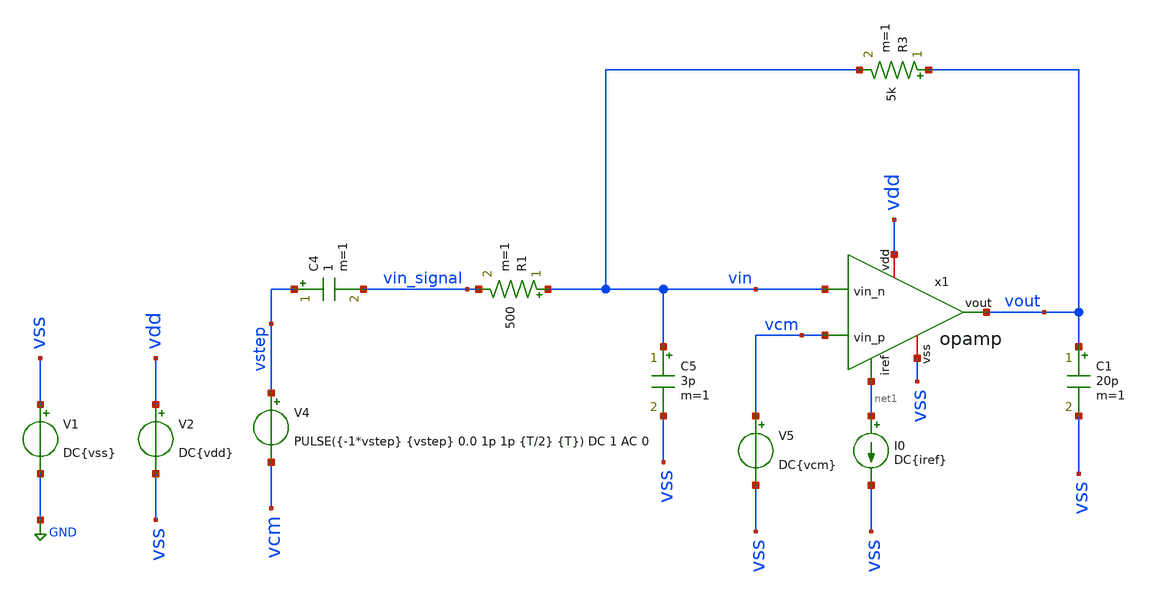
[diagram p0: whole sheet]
** sch_path: opamp/tb_opamp_stepresponse.sch
**.subckt tb_opamp_stepresponse
V1 vss GND DC{vss}
V2 vdd vss DC{vdd}
V4 vstep vcm PULSE({-1*vstep} {vstep} 0.0 1p 1p {T/2} {T}) DC 1 AC 0
C4 vstep vin_signal 1 m=1
I0 net1 vss DC{iref}
R1 vin vin_signal 500 m=1
R3 vout vin 5k m=1
C5 vin vss 3p m=1
C1 vout vss 20p m=1
V5 vcm vss DC{vcm}
x1 vdd net1 vin vcm vout vss opamp
**** begin user architecture code




* Circuit Parameters
.param iref = 100u
.param vdd  = 1.8
.param vss  = 0.0
.param vcm  = 0.8
.param vac  = 10m
.param vstep = 10m
.param T = 20u

.options TEMP = 65.0

* Include Models
*.lib ~/skywater/skywater-pdk/libraries/sky130_fd_pr_ngspice/latest/models/corners/sky130.lib TT
*.lib $env(PDK_ROOT)/$env(PDK)/libs.tech/ngspice/sky130.lib.spice.tt.red tt
.lib /foss/pdks/sky130A/libs.tech/ngspice/sky130.lib.spice.tt.red tt

* OP Parameters & Singals to save
.save all

*Simulations
.control
  set color0 = white

  tran 0.01u 20u
  setplot tran1
  plot v(vstep) v(vin_signal) v(vout)
.endc

.end


**** end user architecture code
**.ends

* expanding   symbol:  opamp.sym # of pins=6
** sym_path: opamp/opamp.sym
** sch_path: opamp/opamp.sch
.subckt opamp vdd iref vin_n vin_p vout vss
*.iopin vdd
*.iopin vss
*.ipin vin_n
*.ipin vin_p
*.ipin iref
*.opin vout
XM3 vbn vbn net1 net1 sky130_fd_pr__nfet_01v8 L=1 W=4 nf=1 ad='W * 0.29' as='W * 0.29' pd='2 * (W + 0.29)'
+ ps='2 * (W + 0.29)' nrd='0.29 / W' nrs='0.29 / W' sa=0 sb=0 sd=0 mult=5 m=5
XM4 voe1 vbn net1 net1 sky130_fd_pr__nfet_01v8 L=1 W=4 nf=1 ad='W * 0.29' as='W * 0.29' pd='2 * (W + 0.29)'
+ ps='2 * (W + 0.29)' nrd='0.29 / W' nrs='0.29 / W' sa=0 sb=0 sd=0 mult=5 m=5
XM5 vp iref vdd vdd sky130_fd_pr__pfet_01v8 L=0.5 W=6 nf=1 ad='W * 0.29' as='W * 0.29' pd='2 * (W + 0.29)'
+ ps='2 * (W + 0.29)' nrd='0.29 / W' nrs='0.29 / W' sa=0 sb=0 sd=0 mult=12 m=12
XM7 vout iref vdd vdd sky130_fd_pr__pfet_01v8 L=0.5 W=8 nf=1 ad='W * 0.29' as='W * 0.29' pd='2 * (W + 0.29)'
+ ps='2 * (W + 0.29)' nrd='0.29 / W' nrs='0.29 / W' sa=0 sb=0 sd=0 mult=50 m=50
XM8 iref iref vdd vdd sky130_fd_pr__pfet_01v8 L=0.5 W=2 nf=1 ad='W * 0.29' as='W * 0.29' pd='2 * (W + 0.29)'
+ ps='2 * (W + 0.29)' nrd='0.29 / W' nrs='0.29 / W' sa=0 sb=0 sd=0 mult=8 m=8
XM9 net2 vdd voe1 vss sky130_fd_pr__nfet_01v8 L=0.15 W=10 nf=1 ad='W * 0.29' as='W * 0.29' pd='2 * (W + 0.29)'
+ ps='2 * (W + 0.29)' nrd='0.29 / W' nrs='0.29 / W' sa=0 sb=0 sd=0 mult=2 m=2
XM6 vout voe1 net1 net1 sky130_fd_pr__nfet_01v8 L=0.5 W=6 nf=1 ad='W * 0.29' as='W * 0.29' pd='2 * (W + 0.29)'
+ ps='2 * (W + 0.29)' nrd='0.29 / W' nrs='0.29 / W' sa=0 sb=0 sd=0 mult=30 m=30
XM1 vbn vin_n vp vp sky130_fd_pr__pfet_01v8_lvt L=1 W=4 nf=1 ad='int((nf+1)/2) * W/nf * 0.29' as='int((nf+2)/2) * W/nf * 0.29'
+ pd='2*int((nf+1)/2) * (W/nf + 0.29)' ps='2*int((nf+2)/2) * (W/nf + 0.29)' nrd='0.29 / W' nrs='0.29 / W'
+ sa=0 sb=0 sd=0 mult=12 m=12
XM2 voe1 vin_p vp vp sky130_fd_pr__pfet_01v8_lvt L=1 W=4 nf=1 ad='int((nf+1)/2) * W/nf * 0.29' as='int((nf+2)/2) * W/nf * 0.29'
+ pd='2*int((nf+1)/2) * (W/nf + 0.29)' ps='2*int((nf+2)/2) * (W/nf + 0.29)' nrd='0.29 / W' nrs='0.29 / W'
+ sa=0 sb=0 sd=0 mult=12 m=12
C1 net2 vout .5p m=1
Vmeas net1 vss 0
.save i(vmeas)
.ends

.GLOBAL GND
.end
